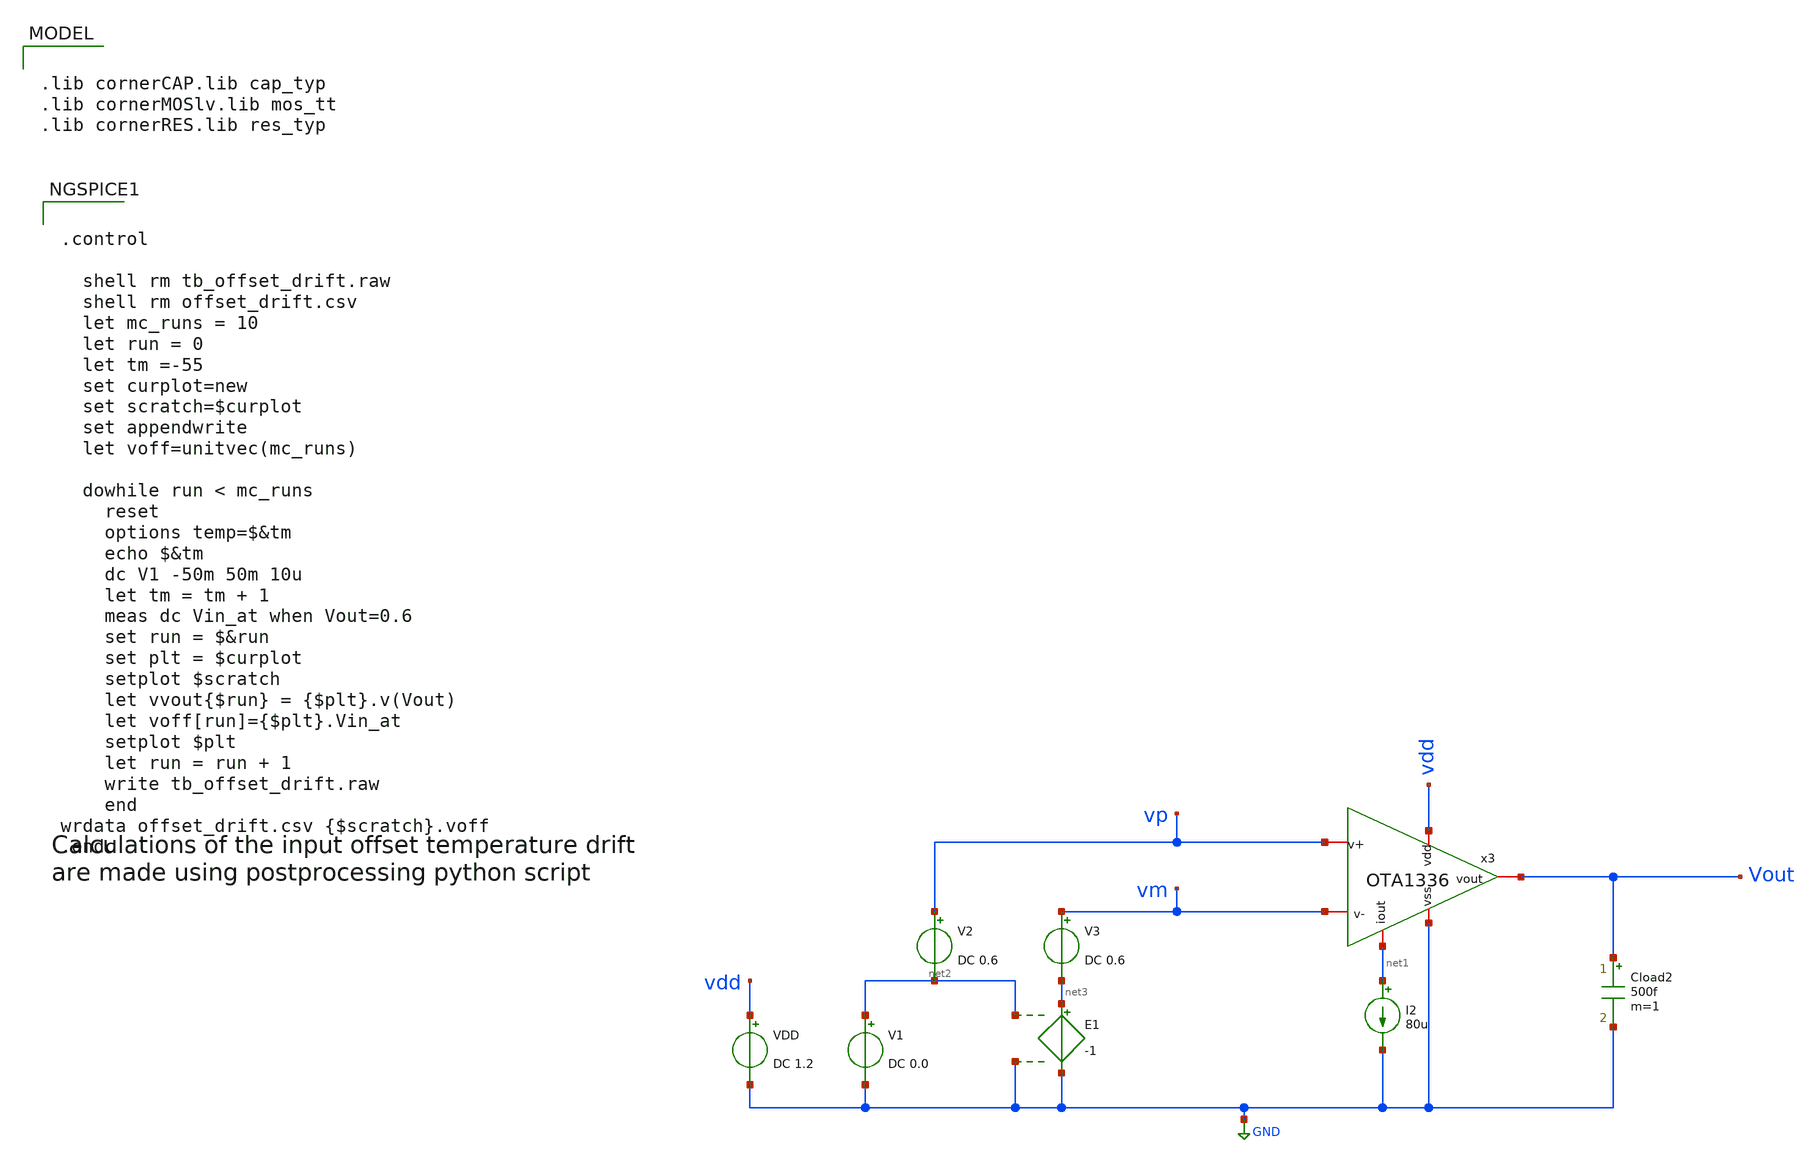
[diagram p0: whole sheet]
** sch_path: OTA1336-main/testbenches/dc/xschem/OTA1336_offset-drift.sch
**.subckt OTA1336_offset-drift
VDD vdd GND DC 1.2
I2 net1 GND 80u
V1 net2 GND DC 0.0
x3 vdd net1 Vout vm vp GND OTA1336
Cload2 Vout GND 500f m=1
V2 vp net2 DC 0.6
V3 vm net3 DC 0.6
E1 net3 GND net2 GND -1
**** begin user architecture code

.lib cornerCAP.lib cap_typ
.lib cornerMOSlv.lib mos_tt
.lib cornerRES.lib res_typ




.control

  shell rm tb_offset_drift.raw
  shell rm offset_drift.csv
  let mc_runs = 10
  let run = 0
  let tm =-55
  set curplot=new
  set scratch=$curplot
  set appendwrite
  let voff=unitvec(mc_runs)

  dowhile run < mc_runs
    reset
    options temp=$&tm
    echo $&tm
    dc V1 -50m 50m 10u
    let tm = tm + 1
    meas dc Vin_at when Vout=0.6
    set run = $&run
    set plt = $curplot
    setplot $scratch
    let vvout{$run} = {$plt}.v(Vout)
    let voff[run]={$plt}.Vin_at
    setplot $plt
    let run = run + 1
    write tb_offset_drift.raw
    end
wrdata offset_drift.csv {$scratch}.voff
.endc


**** end user architecture code
**.ends
.GLOBAL GND
.end
